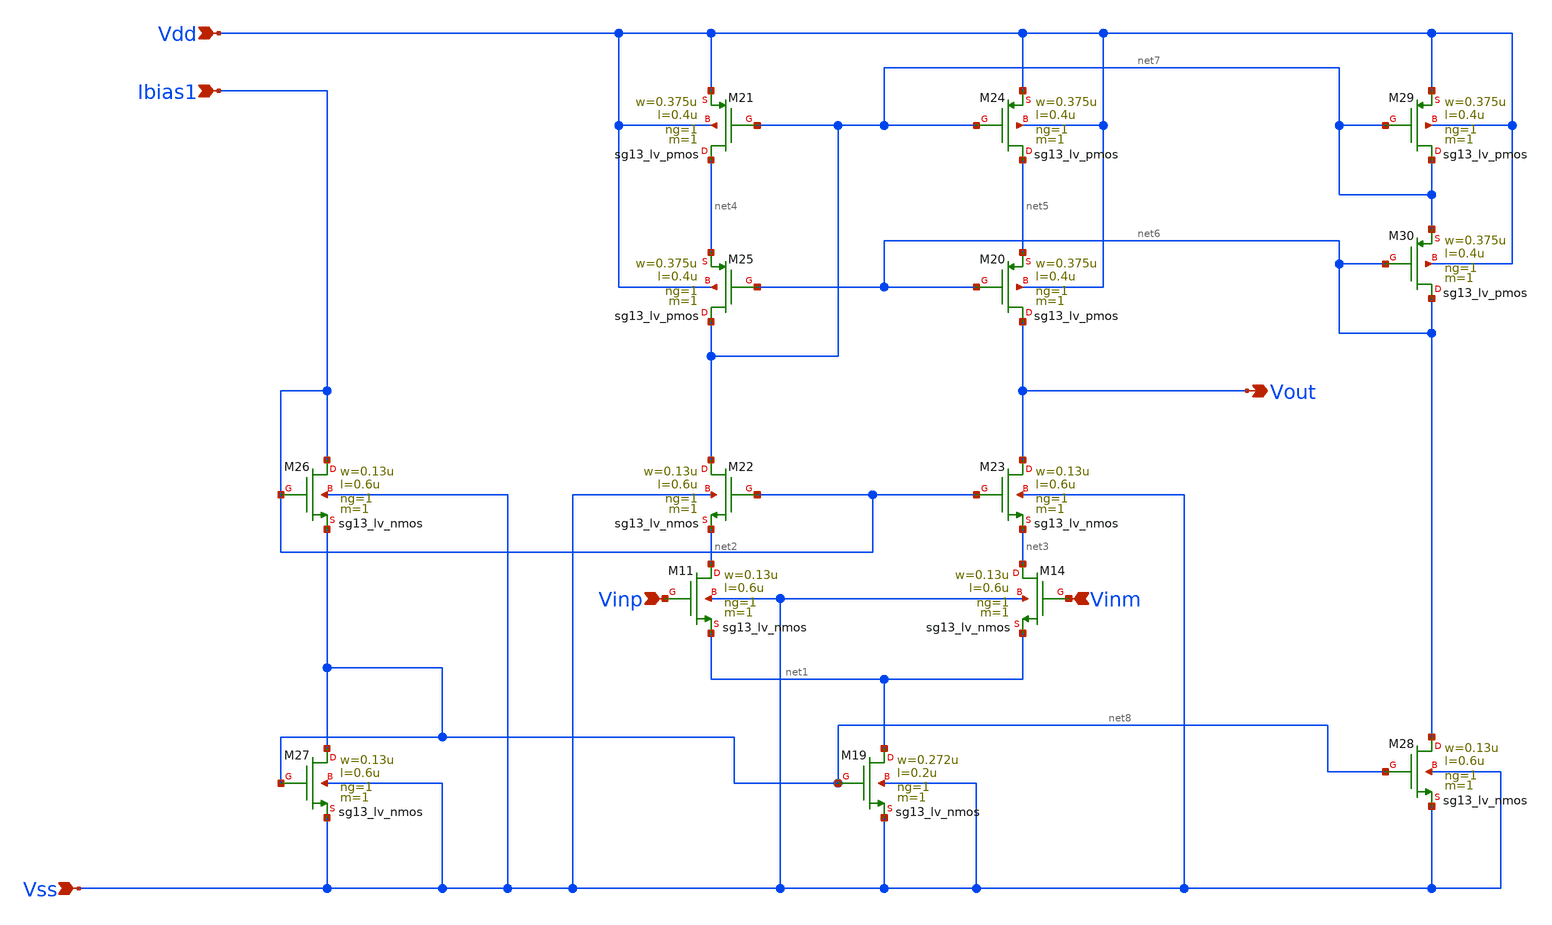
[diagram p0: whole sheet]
** sch_path: DSM/IC_Designs_Hrishi/RealCircuits/Telescopic/Telescopic.sch
* (c) 2024 Hrishikesh, @HSB
**.subckt Telescopic Vinp Vout Vinm Vss Vdd Ibias1
*.ipin Vinp
*.opin Vout
*.ipin Vinm
*.ipin Vss
*.ipin Vdd
*.ipin Ibias1
XM19 net1 net8 Vss Vss sg13_lv_nmos w=0.272u l=0.2u ng=1 m=1 mm_ok=1
XM11 net2 Vinp net1 Vss sg13_lv_nmos w=0.13u l=0.6u ng=1 m=1 mm_ok=1
XM26 Ibias1 Ibias1 net8 Vss sg13_lv_nmos w=0.13u l=0.6u ng=1 m=1 mm_ok=1
XM27 net8 net8 Vss Vss sg13_lv_nmos w=0.13u l=0.6u ng=1 m=1 mm_ok=1
XM28 net6 net8 Vss Vss sg13_lv_nmos w=0.13u l=0.6u ng=1 m=1 mm_ok=1
XM23 Vout Ibias1 net3 Vss sg13_lv_nmos w=0.13u l=0.6u ng=1 m=1 mm_ok=1
XM14 net3 Vinm net1 Vss sg13_lv_nmos w=0.13u l=0.6u ng=1 m=1 mm_ok=1
XM22 net7 Ibias1 net2 Vss sg13_lv_nmos w=0.13u l=0.6u ng=1 m=1 mm_ok=1
XM29 net7 net7 Vdd Vdd sg13_lv_pmos w=0.375u l=0.4u ng=1 m=1 mm_ok=1
XM30 net6 net6 net7 Vdd sg13_lv_pmos w=0.375u l=0.4u ng=1 m=1 mm_ok=1
XM20 Vout net6 net5 Vdd sg13_lv_pmos w=0.375u l=0.4u ng=1 m=1 mm_ok=1
XM24 net5 net7 Vdd Vdd sg13_lv_pmos w=0.375u l=0.4u ng=1 m=1 mm_ok=1
XM21 net4 net7 Vdd Vdd sg13_lv_pmos w=0.375u l=0.4u ng=1 m=1 mm_ok=1
XM25 net7 net6 net4 Vdd sg13_lv_pmos w=0.375u l=0.4u ng=1 m=1 mm_ok=1
**.ends
.end
